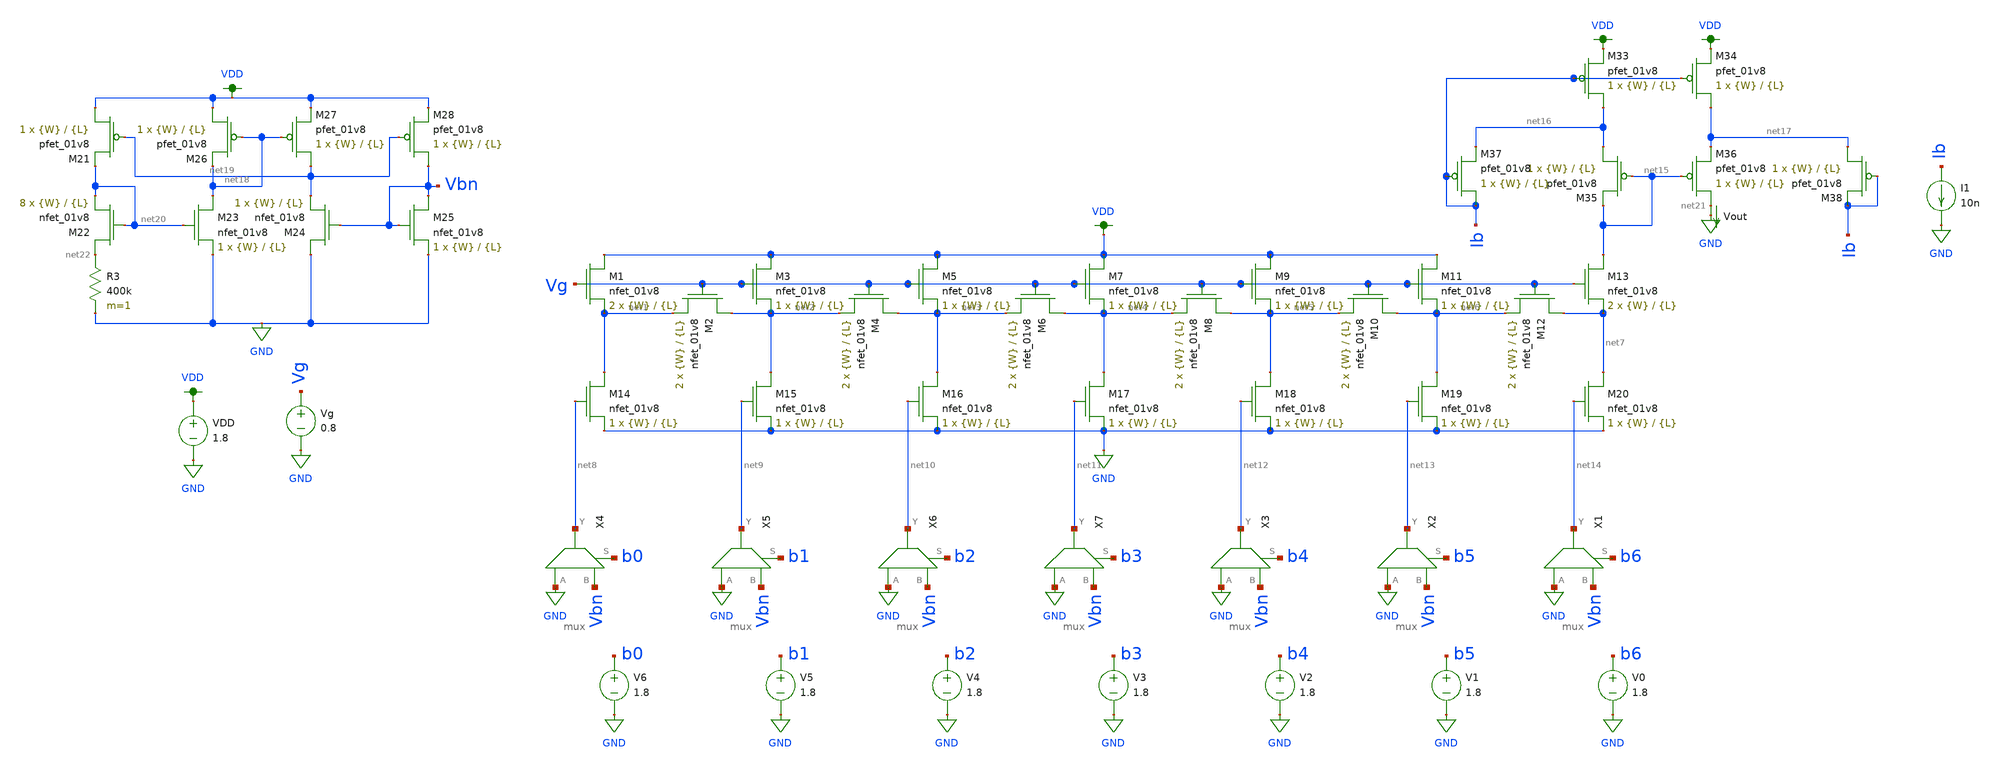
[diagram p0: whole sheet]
** sch_path: schematics/dac_dnl_inl_current_mirror.sch
**.subckt dac_dnl_inl_current_mirror
XM1 VDD Vg net1 GND sky130_fd_pr__nfet_01v8 L={L} W={W} nf=1 ad='int((nf+1)/2) * W/nf * 0.29' as='int((nf+2)/2) * W/nf * 0.29'
+ pd='2*int((nf+1)/2) * (W/nf + 0.29)' ps='2*int((nf+2)/2) * (W/nf + 0.29)' nrd='0.29 / W' nrs='0.29 / W'
+ sa=0 sb=0 sd=0 mult=2 m=2
XM2 net2 Vg net1 GND sky130_fd_pr__nfet_01v8 L={L} W={W} nf=1 ad='int((nf+1)/2) * W/nf * 0.29' as='int((nf+2)/2) * W/nf * 0.29'
+ pd='2*int((nf+1)/2) * (W/nf + 0.29)' ps='2*int((nf+2)/2) * (W/nf + 0.29)' nrd='0.29 / W' nrs='0.29 / W'
+ sa=0 sb=0 sd=0 mult=2 m=2
XM3 VDD Vg net2 GND sky130_fd_pr__nfet_01v8 L={L} W={W} nf=1 ad='int((nf+1)/2) * W/nf * 0.29' as='int((nf+2)/2) * W/nf * 0.29'
+ pd='2*int((nf+1)/2) * (W/nf + 0.29)' ps='2*int((nf+2)/2) * (W/nf + 0.29)' nrd='0.29 / W' nrs='0.29 / W'
+ sa=0 sb=0 sd=0 mult=1 m=1
XM4 net3 Vg net2 GND sky130_fd_pr__nfet_01v8 L={L} W={W} nf=1 ad='int((nf+1)/2) * W/nf * 0.29' as='int((nf+2)/2) * W/nf * 0.29'
+ pd='2*int((nf+1)/2) * (W/nf + 0.29)' ps='2*int((nf+2)/2) * (W/nf + 0.29)' nrd='0.29 / W' nrs='0.29 / W'
+ sa=0 sb=0 sd=0 mult=2 m=2
XM5 VDD Vg net3 GND sky130_fd_pr__nfet_01v8 L={L} W={W} nf=1 ad='int((nf+1)/2) * W/nf * 0.29' as='int((nf+2)/2) * W/nf * 0.29'
+ pd='2*int((nf+1)/2) * (W/nf + 0.29)' ps='2*int((nf+2)/2) * (W/nf + 0.29)' nrd='0.29 / W' nrs='0.29 / W'
+ sa=0 sb=0 sd=0 mult=1 m=1
XM6 net4 Vg net3 GND sky130_fd_pr__nfet_01v8 L={L} W={W} nf=1 ad='int((nf+1)/2) * W/nf * 0.29' as='int((nf+2)/2) * W/nf * 0.29'
+ pd='2*int((nf+1)/2) * (W/nf + 0.29)' ps='2*int((nf+2)/2) * (W/nf + 0.29)' nrd='0.29 / W' nrs='0.29 / W'
+ sa=0 sb=0 sd=0 mult=2 m=2
XM7 VDD Vg net4 GND sky130_fd_pr__nfet_01v8 L={L} W={W} nf=1 ad='int((nf+1)/2) * W/nf * 0.29' as='int((nf+2)/2) * W/nf * 0.29'
+ pd='2*int((nf+1)/2) * (W/nf + 0.29)' ps='2*int((nf+2)/2) * (W/nf + 0.29)' nrd='0.29 / W' nrs='0.29 / W'
+ sa=0 sb=0 sd=0 mult=1 m=1
XM8 net5 Vg net4 GND sky130_fd_pr__nfet_01v8 L={L} W={W} nf=1 ad='int((nf+1)/2) * W/nf * 0.29' as='int((nf+2)/2) * W/nf * 0.29'
+ pd='2*int((nf+1)/2) * (W/nf + 0.29)' ps='2*int((nf+2)/2) * (W/nf + 0.29)' nrd='0.29 / W' nrs='0.29 / W'
+ sa=0 sb=0 sd=0 mult=2 m=2
XM9 VDD Vg net5 GND sky130_fd_pr__nfet_01v8 L={L} W={W} nf=1 ad='int((nf+1)/2) * W/nf * 0.29' as='int((nf+2)/2) * W/nf * 0.29'
+ pd='2*int((nf+1)/2) * (W/nf + 0.29)' ps='2*int((nf+2)/2) * (W/nf + 0.29)' nrd='0.29 / W' nrs='0.29 / W'
+ sa=0 sb=0 sd=0 mult=1 m=1
XM10 net6 Vg net5 GND sky130_fd_pr__nfet_01v8 L={L} W={W} nf=1 ad='int((nf+1)/2) * W/nf * 0.29' as='int((nf+2)/2) * W/nf * 0.29'
+ pd='2*int((nf+1)/2) * (W/nf + 0.29)' ps='2*int((nf+2)/2) * (W/nf + 0.29)' nrd='0.29 / W' nrs='0.29 / W'
+ sa=0 sb=0 sd=0 mult=2 m=2
XM11 VDD Vg net6 GND sky130_fd_pr__nfet_01v8 L={L} W={W} nf=1 ad='int((nf+1)/2) * W/nf * 0.29' as='int((nf+2)/2) * W/nf * 0.29'
+ pd='2*int((nf+1)/2) * (W/nf + 0.29)' ps='2*int((nf+2)/2) * (W/nf + 0.29)' nrd='0.29 / W' nrs='0.29 / W'
+ sa=0 sb=0 sd=0 mult=1 m=1
XM12 net7 Vg net6 GND sky130_fd_pr__nfet_01v8 L={L} W={W} nf=1 ad='int((nf+1)/2) * W/nf * 0.29' as='int((nf+2)/2) * W/nf * 0.29'
+ pd='2*int((nf+1)/2) * (W/nf + 0.29)' ps='2*int((nf+2)/2) * (W/nf + 0.29)' nrd='0.29 / W' nrs='0.29 / W'
+ sa=0 sb=0 sd=0 mult=2 m=2
XM13 net15 Vg net7 GND sky130_fd_pr__nfet_01v8 L={L} W={W} nf=1 ad='int((nf+1)/2) * W/nf * 0.29' as='int((nf+2)/2) * W/nf * 0.29'
+ pd='2*int((nf+1)/2) * (W/nf + 0.29)' ps='2*int((nf+2)/2) * (W/nf + 0.29)' nrd='0.29 / W' nrs='0.29 / W'
+ sa=0 sb=0 sd=0 mult=2 m=2
XM14 net1 net8 GND GND sky130_fd_pr__nfet_01v8 L={L} W={W} nf=1 ad='int((nf+1)/2) * W/nf * 0.29' as='int((nf+2)/2) * W/nf * 0.29'
+ pd='2*int((nf+1)/2) * (W/nf + 0.29)' ps='2*int((nf+2)/2) * (W/nf + 0.29)' nrd='0.29 / W' nrs='0.29 / W'
+ sa=0 sb=0 sd=0 mult=1 m=1
XM15 net2 net9 GND GND sky130_fd_pr__nfet_01v8 L={L} W={W} nf=1 ad='int((nf+1)/2) * W/nf * 0.29' as='int((nf+2)/2) * W/nf * 0.29'
+ pd='2*int((nf+1)/2) * (W/nf + 0.29)' ps='2*int((nf+2)/2) * (W/nf + 0.29)' nrd='0.29 / W' nrs='0.29 / W'
+ sa=0 sb=0 sd=0 mult=1 m=1
XM16 net3 net10 GND GND sky130_fd_pr__nfet_01v8 L={L} W={W} nf=1 ad='int((nf+1)/2) * W/nf * 0.29' as='int((nf+2)/2) * W/nf * 0.29'
+ pd='2*int((nf+1)/2) * (W/nf + 0.29)' ps='2*int((nf+2)/2) * (W/nf + 0.29)' nrd='0.29 / W' nrs='0.29 / W'
+ sa=0 sb=0 sd=0 mult=1 m=1
XM17 net4 net11 GND GND sky130_fd_pr__nfet_01v8 L={L} W={W} nf=1 ad='int((nf+1)/2) * W/nf * 0.29' as='int((nf+2)/2) * W/nf * 0.29'
+ pd='2*int((nf+1)/2) * (W/nf + 0.29)' ps='2*int((nf+2)/2) * (W/nf + 0.29)' nrd='0.29 / W' nrs='0.29 / W'
+ sa=0 sb=0 sd=0 mult=1 m=1
XM18 net5 net12 GND GND sky130_fd_pr__nfet_01v8 L={L} W={W} nf=1 ad='int((nf+1)/2) * W/nf * 0.29' as='int((nf+2)/2) * W/nf * 0.29'
+ pd='2*int((nf+1)/2) * (W/nf + 0.29)' ps='2*int((nf+2)/2) * (W/nf + 0.29)' nrd='0.29 / W' nrs='0.29 / W'
+ sa=0 sb=0 sd=0 mult=1 m=1
XM19 net6 net13 GND GND sky130_fd_pr__nfet_01v8 L={L} W={W} nf=1 ad='int((nf+1)/2) * W/nf * 0.29' as='int((nf+2)/2) * W/nf * 0.29'
+ pd='2*int((nf+1)/2) * (W/nf + 0.29)' ps='2*int((nf+2)/2) * (W/nf + 0.29)' nrd='0.29 / W' nrs='0.29 / W'
+ sa=0 sb=0 sd=0 mult=1 m=1
XM20 net7 net14 GND GND sky130_fd_pr__nfet_01v8 L={L} W={W} nf=1 ad='int((nf+1)/2) * W/nf * 0.29' as='int((nf+2)/2) * W/nf * 0.29'
+ pd='2*int((nf+1)/2) * (W/nf + 0.29)' ps='2*int((nf+2)/2) * (W/nf + 0.29)' nrd='0.29 / W' nrs='0.29 / W'
+ sa=0 sb=0 sd=0 mult=1 m=1
V0 b6 GND 1.8
V1 b5 GND 1.8
V2 b4 GND 1.8
V3 b3 GND 1.8
V4 b2 GND 1.8
V5 b1 GND 1.8
V6 b0 GND 1.8
Vout net21 GND 0
.save i(vout)
VDD VDD GND 1.8
X4 GND Vbn net8 b0 mux
X5 GND Vbn net9 b1 mux
X6 GND Vbn net10 b2 mux
X7 GND Vbn net11 b3 mux
X3 GND Vbn net12 b4 mux
X2 GND Vbn net13 b5 mux
X1 GND Vbn net14 b6 mux
XM33 net16 Ib VDD VDD sky130_fd_pr__pfet_01v8 L={L} W={W} nf=1 ad='int((nf+1)/2) * W/nf * 0.29' as='int((nf+2)/2) * W/nf * 0.29'
+ pd='2*int((nf+1)/2) * (W/nf + 0.29)' ps='2*int((nf+2)/2) * (W/nf + 0.29)' nrd='0.29 / W' nrs='0.29 / W'
+ sa=0 sb=0 sd=0 mult=1 m=1
XM34 net17 Ib VDD VDD sky130_fd_pr__pfet_01v8 L={L} W={W} nf=1 ad='int((nf+1)/2) * W/nf * 0.29' as='int((nf+2)/2) * W/nf * 0.29'
+ pd='2*int((nf+1)/2) * (W/nf + 0.29)' ps='2*int((nf+2)/2) * (W/nf + 0.29)' nrd='0.29 / W' nrs='0.29 / W'
+ sa=0 sb=0 sd=0 mult=1 m=1
XM35 net16 net15 net15 VDD sky130_fd_pr__pfet_01v8 L={L} W={W} nf=1 ad='int((nf+1)/2) * W/nf * 0.29'
+ as='int((nf+2)/2) * W/nf * 0.29' pd='2*int((nf+1)/2) * (W/nf + 0.29)' ps='2*int((nf+2)/2) * (W/nf + 0.29)'
+ nrd='0.29 / W' nrs='0.29 / W' sa=0 sb=0 sd=0 mult=1 m=1
XM36 net21 net15 net17 VDD sky130_fd_pr__pfet_01v8 L={L} W={W} nf=1 ad='int((nf+1)/2) * W/nf * 0.29'
+ as='int((nf+2)/2) * W/nf * 0.29' pd='2*int((nf+1)/2) * (W/nf + 0.29)' ps='2*int((nf+2)/2) * (W/nf + 0.29)'
+ nrd='0.29 / W' nrs='0.29 / W' sa=0 sb=0 sd=0 mult=1 m=1
XM37 Ib Ib net16 VDD sky130_fd_pr__pfet_01v8 L={L} W={W} nf=1 ad='int((nf+1)/2) * W/nf * 0.29' as='int((nf+2)/2) * W/nf * 0.29'
+ pd='2*int((nf+1)/2) * (W/nf + 0.29)' ps='2*int((nf+2)/2) * (W/nf + 0.29)' nrd='0.29 / W' nrs='0.29 / W'
+ sa=0 sb=0 sd=0 mult=1 m=1
XM38 net17 Ib Ib VDD sky130_fd_pr__pfet_01v8 L={L} W={W} nf=1 ad='int((nf+1)/2) * W/nf * 0.29' as='int((nf+2)/2) * W/nf * 0.29'
+ pd='2*int((nf+1)/2) * (W/nf + 0.29)' ps='2*int((nf+2)/2) * (W/nf + 0.29)' nrd='0.29 / W' nrs='0.29 / W'
+ sa=0 sb=0 sd=0 mult=1 m=1
XM21 VDD net19 net20 VDD sky130_fd_pr__pfet_01v8 L={L} W={W} nf=1 ad='int((nf+1)/2) * W/nf * 0.29' as='int((nf+2)/2) * W/nf * 0.29'
+ pd='2*int((nf+1)/2) * (W/nf + 0.29)' ps='2*int((nf+2)/2) * (W/nf + 0.29)' nrd='0.29 / W' nrs='0.29 / W'
+ sa=0 sb=0 sd=0 mult=1 m=1
XM22 net22 net20 net20 GND sky130_fd_pr__nfet_01v8 L={L} W={W} nf=1 ad='int((nf+1)/2) * W/nf * 0.29'
+ as='int((nf+2)/2) * W/nf * 0.29' pd='2*int((nf+1)/2) * (W/nf + 0.29)' ps='2*int((nf+2)/2) * (W/nf + 0.29)'
+ nrd='0.29 / W' nrs='0.29 / W' sa=0 sb=0 sd=0 mult=8 m=8
R3 net22 GND 400k m=1
XM23 net18 net20 GND GND sky130_fd_pr__nfet_01v8 L={L} W={W} nf=1 ad='int((nf+1)/2) * W/nf * 0.29' as='int((nf+2)/2) * W/nf * 0.29'
+ pd='2*int((nf+1)/2) * (W/nf + 0.29)' ps='2*int((nf+2)/2) * (W/nf + 0.29)' nrd='0.29 / W' nrs='0.29 / W'
+ sa=0 sb=0 sd=0 mult=1 m=1
XM24 GND Vbn net19 GND sky130_fd_pr__nfet_01v8 L={L} W={W} nf=1 ad='int((nf+1)/2) * W/nf * 0.29' as='int((nf+2)/2) * W/nf * 0.29'
+ pd='2*int((nf+1)/2) * (W/nf + 0.29)' ps='2*int((nf+2)/2) * (W/nf + 0.29)' nrd='0.29 / W' nrs='0.29 / W'
+ sa=0 sb=0 sd=0 mult=1 m=1
XM25 Vbn Vbn GND GND sky130_fd_pr__nfet_01v8 L={L} W={W} nf=1 ad='int((nf+1)/2) * W/nf * 0.29' as='int((nf+2)/2) * W/nf * 0.29'
+ pd='2*int((nf+1)/2) * (W/nf + 0.29)' ps='2*int((nf+2)/2) * (W/nf + 0.29)' nrd='0.29 / W' nrs='0.29 / W'
+ sa=0 sb=0 sd=0 mult=1 m=1
XM26 VDD net18 net18 VDD sky130_fd_pr__pfet_01v8 L={L} W={W} nf=1 ad='int((nf+1)/2) * W/nf * 0.29' as='int((nf+2)/2) * W/nf * 0.29'
+ pd='2*int((nf+1)/2) * (W/nf + 0.29)' ps='2*int((nf+2)/2) * (W/nf + 0.29)' nrd='0.29 / W' nrs='0.29 / W'
+ sa=0 sb=0 sd=0 mult=1 m=1
XM27 net19 net18 VDD VDD sky130_fd_pr__pfet_01v8 L={L} W={W} nf=1 ad='int((nf+1)/2) * W/nf * 0.29' as='int((nf+2)/2) * W/nf * 0.29'
+ pd='2*int((nf+1)/2) * (W/nf + 0.29)' ps='2*int((nf+2)/2) * (W/nf + 0.29)' nrd='0.29 / W' nrs='0.29 / W'
+ sa=0 sb=0 sd=0 mult=1 m=1
XM28 Vbn net19 VDD VDD sky130_fd_pr__pfet_01v8 L={L} W={W} nf=1 ad='int((nf+1)/2) * W/nf * 0.29' as='int((nf+2)/2) * W/nf * 0.29'
+ pd='2*int((nf+1)/2) * (W/nf + 0.29)' ps='2*int((nf+2)/2) * (W/nf + 0.29)' nrd='0.29 / W' nrs='0.29 / W'
+ sa=0 sb=0 sd=0 mult=1 m=1
I1 Ib GND 10n
Vg Vg GND 0.8
**** begin user architecture code

.param W=1
.param L=4
.control
set wr_vecnames
set wr_singlescale
let code = 0
  while code < 128
    if code eq 0
      let b0 = 0
    else
      let b0 = code % 2
    end
    if floor(code / 2) eq 0
      let b1 = 0
    else
      let b1 = floor(code / 2) % 2
    end
    if floor(code / 4) eq 0
      let b2 = 0
    else
      let b2 = floor(code / 4) % 2
    end
    if floor(code / 8) eq 0
      let b3 = 0
    else
      let b3 = floor(code / 8) % 2
    end
    if floor(code / 16) eq 0
      let b4 = 0
    else
      let b4 = floor(code / 16) % 2
    end
    if floor(code / 32) eq 0
      let b5 = 0
    else
      let b5 = floor(code / 32) % 2
    end
    if floor(code / 64) eq 0
      let b6 = 0
    else
      let b6 = floor(code / 64) % 2
    end
    alter v0 $&b0
    alter v1 $&b1
    alter v2 $&b2
    alter v3 $&b3
    alter v4 $&b4
    alter v5 $&b5
    alter v6 $&b6
    save all
    op
    wrdata ~/current-output-dac-vlsi/simulations/dac_sim.txt i(Vout) v(b5) v(b6)
    if code eq 0
      set appendwrite
      set wr_vecnames = FALSE
    end
    let code = code + 1
  end
.endc


.option wnflag=1
.param MC_SWITCH=0.0
.lib ~/skywater/skywater-pdk/libraries/sky130_fd_pr_ngspice/latest/models/sky130.lib.spice tt

**** end user architecture code
**.ends

* expanding   symbol:  /home/madvlsi/current-output-dac-vlsi/schematics/mux.sym # of pins=4
** sym_path: /home/madvlsi/current-output-dac-vlsi/schematics/mux.sym
** sch_path: /home/madvlsi/current-output-dac-vlsi/schematics/mux.sch
.subckt mux A B Y S
*.ipin S
*.ipin A
*.opin Y
*.ipin B
XM1 net1 S GND GND sky130_fd_pr__nfet_01v8 L=0.15 W=1 nf=1 ad='int((nf+1)/2) * W/nf * 0.29' as='int((nf+2)/2) * W/nf * 0.29'
+ pd='2*int((nf+1)/2) * (W/nf + 0.29)' ps='2*int((nf+2)/2) * (W/nf + 0.29)' nrd='0.29 / W' nrs='0.29 / W'
+ sa=0 sb=0 sd=0 mult=1 m=1
XM2 net1 S VDD VDD sky130_fd_pr__pfet_01v8 L=0.15 W=1 nf=1 ad='int((nf+1)/2) * W/nf * 0.29' as='int((nf+2)/2) * W/nf * 0.29'
+ pd='2*int((nf+1)/2) * (W/nf + 0.29)' ps='2*int((nf+2)/2) * (W/nf + 0.29)' nrd='0.29 / W' nrs='0.29 / W'
+ sa=0 sb=0 sd=0 mult=1 m=1
XM3 Y S B GND sky130_fd_pr__nfet_01v8 L=0.15 W=1 nf=1 ad='int((nf+1)/2) * W/nf * 0.29' as='int((nf+2)/2) * W/nf * 0.29'
+ pd='2*int((nf+1)/2) * (W/nf + 0.29)' ps='2*int((nf+2)/2) * (W/nf + 0.29)' nrd='0.29 / W' nrs='0.29 / W'
+ sa=0 sb=0 sd=0 mult=1 m=1
XM4 A net1 Y GND sky130_fd_pr__nfet_01v8 L=0.15 W=1 nf=1 ad='int((nf+1)/2) * W/nf * 0.29' as='int((nf+2)/2) * W/nf * 0.29'
+ pd='2*int((nf+1)/2) * (W/nf + 0.29)' ps='2*int((nf+2)/2) * (W/nf + 0.29)' nrd='0.29 / W' nrs='0.29 / W'
+ sa=0 sb=0 sd=0 mult=1 m=1
.ends

.GLOBAL GND
.GLOBAL VDD
.end
